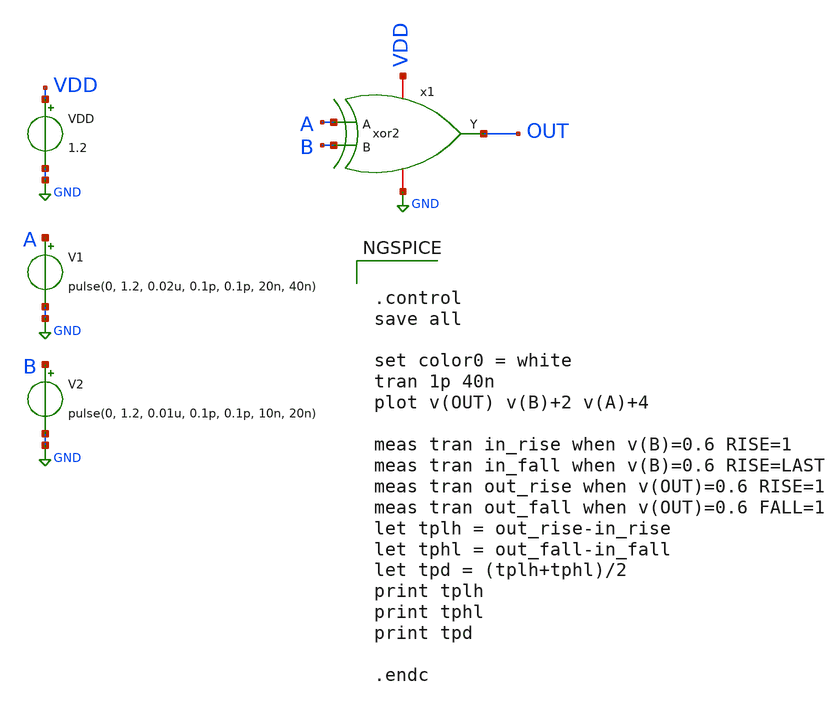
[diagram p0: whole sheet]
** sch_path: design/ALU/xor2_tb.sch
**.subckt xor2_tb
VDD VDD GND 1.2
V1 A GND pulse(0, 1.2, 0.02u, 0.1p, 0.1p, 20n, 40n)
V2 B GND pulse(0, 1.2, 0.01u, 0.1p, 0.1p, 10n, 20n)
x1 OUT A VDD GND B xor2
**** begin user architecture code

** opencircuitdesign pdks install
.lib $::SKYWATER_MODELS/sky130.lib.spice tt_mm




.control
save all

set color0 = white
tran 1p 40n
plot v(OUT) v(B)+2 v(A)+4

meas tran in_rise when v(B)=0.6 RISE=1
meas tran in_fall when v(B)=0.6 RISE=LAST
meas tran out_rise when v(OUT)=0.6 RISE=1
meas tran out_fall when v(OUT)=0.6 FALL=1
let tplh = out_rise-in_rise
let tphl = out_fall-in_fall
let tpd = (tplh+tphl)/2
print tplh
print tphl
print tpd

.endc

**** end user architecture code
**.ends
.GLOBAL GND
.end
